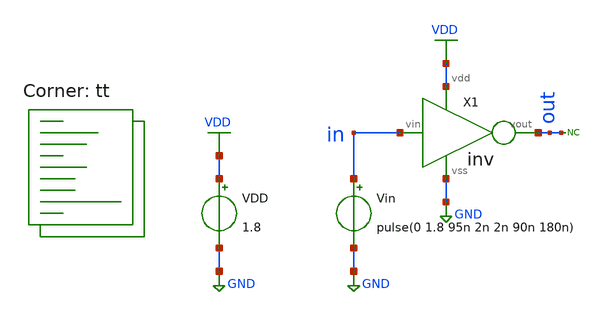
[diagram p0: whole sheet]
** sch_path: xsch/tb/inv/tb_inv_tran.sch
**.subckt tb_inv_tran
Vin in GND pulse(0 1.8 95n 2n 2n 90n 180n)
VDD VDD GND 1.8
X1 in out VDD GND inv
* noconn out
**** begin user architecture code



* control language script

.control
tran 100p 500n               ; simulation command 1

set xbrushwidth=2
plot v(in) v(out)

write $inputdir/outtran.out v(in) v(out)

reset

dc vin 0 2 0.01              ; simulation command 2

plot v(out)                  ; v(in) not required because it is the x axis already

write $inputdir/outdc.out v(out)

.endc
.end



.lib $::SKYWATER_MODELS/sky130.lib.spice tt
**** end user architecture code
**.ends
.GLOBAL VDD
.GLOBAL GND
.end
